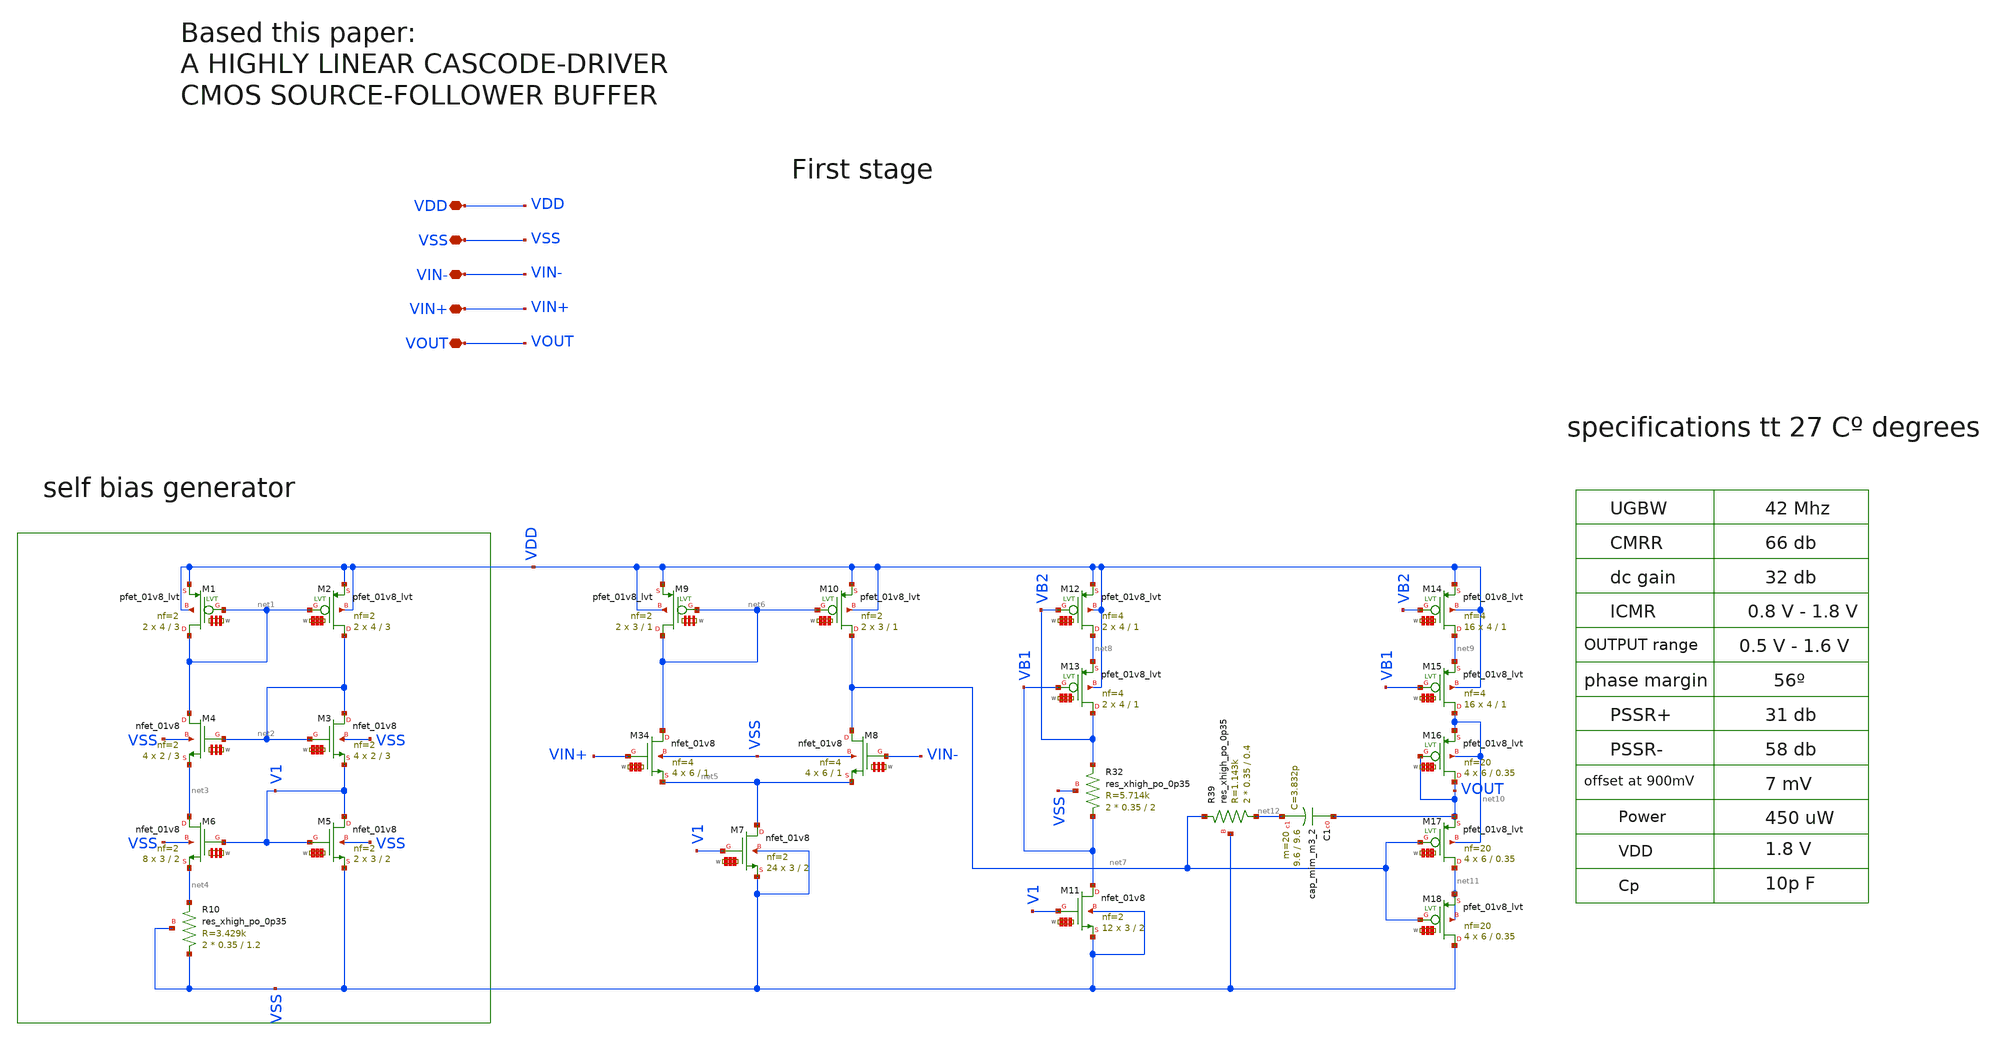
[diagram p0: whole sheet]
** sch_path: my_ip/LIB/Sky130A/single ended amplifiers/VA003_NMOS_1.8_sky130A.sch
**.subckt VA003_NMOS_1.8_sky130A VDD VSS VIN- VIN+ VOUT
*.iopin VDD
*.iopin VSS
*.iopin VIN-
*.iopin VIN+
*.iopin VOUT
XR10 VSS net4 VSS sky130_fd_pr__res_xhigh_po_0p35 L=1.2 mult=2 m=2
XM4 net1 net2 net3 VSS sky130_fd_pr__nfet_01v8 L=3 W='2 * 2 ' nf=2 ad='int((2 + 1)/2) * 2 / 2 * 0.29'
+ as='int((2 + 2)/2) * 2 / 2 * 0.29' pd='2*int((2 + 1)/2) * (2 / 2 + 0.29)' ps='2*int((2 + 2)/2) * (2 / 2 + 0.29)'
+ nrd='0.29 / 2 ' nrs='0.29 / 2 ' sa=0 sb=0 sd=0 mult=4 m=4
XM3 net2 net2 V1 VSS sky130_fd_pr__nfet_01v8 L=3 W='2 * 2 ' nf=2 ad='int((2 + 1)/2) * 2 / 2 * 0.29' as='int((2 + 2)/2) * 2 / 2 * 0.29'
+ pd='2*int((2 + 1)/2) * (2 / 2 + 0.29)' ps='2*int((2 + 2)/2) * (2 / 2 + 0.29)' nrd='0.29 / 2 ' nrs='0.29 / 2 '
+ sa=0 sb=0 sd=0 mult=4 m=4
XM6 net3 V1 net4 VSS sky130_fd_pr__nfet_01v8 L=2 W='3 * 2 ' nf=2 ad='int((2 + 1)/2) * 3 / 2 * 0.29' as='int((2 + 2)/2) * 3 / 2 * 0.29'
+ pd='2*int((2 + 1)/2) * (3 / 2 + 0.29)' ps='2*int((2 + 2)/2) * (3 / 2 + 0.29)' nrd='0.29 / 3 ' nrs='0.29 / 3 '
+ sa=0 sb=0 sd=0 mult=8 m=8
XM5 V1 V1 VSS VSS sky130_fd_pr__nfet_01v8 L=2 W='3 * 2 ' nf=2 ad='int((2 + 1)/2) * 3 / 2 * 0.29' as='int((2 + 2)/2) * 3 / 2 * 0.29'
+ pd='2*int((2 + 1)/2) * (3 / 2 + 0.29)' ps='2*int((2 + 2)/2) * (3 / 2 + 0.29)' nrd='0.29 / 3 ' nrs='0.29 / 3 '
+ sa=0 sb=0 sd=0 mult=2 m=2
XM2 net2 net1 VDD VDD sky130_fd_pr__pfet_01v8_lvt L=3 W='4 * 2 ' nf=2 ad='int((2 + 1)/2) * 4 / 2 * 0.29'
+ as='int((2 + 2)/2) * 4 / 2 * 0.29' pd='2*int((2 + 1)/2) * (4 / 2 + 0.29)' ps='2*int((2 + 2)/2) * (4 / 2 + 0.29)'
+ nrd='0.29 / 4 ' nrs='0.29 / 4 ' sa=0 sb=0 sd=0 mult=2 m=2
XM1 net1 net1 VDD VDD sky130_fd_pr__pfet_01v8_lvt L=3 W='4 * 2 ' nf=2 ad='int((2 + 1)/2) * 4 / 2 * 0.29'
+ as='int((2 + 2)/2) * 4 / 2 * 0.29' pd='2*int((2 + 1)/2) * (4 / 2 + 0.29)' ps='2*int((2 + 2)/2) * (4 / 2 + 0.29)'
+ nrd='0.29 / 4 ' nrs='0.29 / 4 ' sa=0 sb=0 sd=0 mult=2 m=2
XM7 net5 V1 VSS VSS sky130_fd_pr__nfet_01v8 L=2 W='3 * 2 ' nf=2 ad='int((2 + 1)/2) * 3 / 2 * 0.29' as='int((2 + 2)/2) * 3 / 2 * 0.29'
+ pd='2*int((2 + 1)/2) * (3 / 2 + 0.29)' ps='2*int((2 + 2)/2) * (3 / 2 + 0.29)' nrd='0.29 / 3 ' nrs='0.29 / 3 '
+ sa=0 sb=0 sd=0 mult=24 m=24
XM34 net6 VIN+ net5 VSS sky130_fd_pr__nfet_01v8 L=1 W='6 * 4 ' nf=4 ad='int((4 + 1)/2) * 6 / 4 * 0.29'
+ as='int((4 + 2)/2) * 6 / 4 * 0.29' pd='2*int((4 + 1)/2) * (6 / 4 + 0.29)' ps='2*int((4 + 2)/2) * (6 / 4 + 0.29)'
+ nrd='0.29 / 6 ' nrs='0.29 / 6 ' sa=0 sb=0 sd=0 mult=4 m=4
XM8 net7 VIN- net5 VSS sky130_fd_pr__nfet_01v8 L=1 W='6 * 4 ' nf=4 ad='int((4 + 1)/2) * 6 / 4 * 0.29'
+ as='int((4 + 2)/2) * 6 / 4 * 0.29' pd='2*int((4 + 1)/2) * (6 / 4 + 0.29)' ps='2*int((4 + 2)/2) * (6 / 4 + 0.29)'
+ nrd='0.29 / 6 ' nrs='0.29 / 6 ' sa=0 sb=0 sd=0 mult=4 m=4
XM9 net6 net6 VDD VDD sky130_fd_pr__pfet_01v8_lvt L=1 W='3 * 2 ' nf=2 ad='int((2 + 1)/2) * 3 / 2 * 0.29'
+ as='int((2 + 2)/2) * 3 / 2 * 0.29' pd='2*int((2 + 1)/2) * (3 / 2 + 0.29)' ps='2*int((2 + 2)/2) * (3 / 2 + 0.29)'
+ nrd='0.29 / 3 ' nrs='0.29 / 3 ' sa=0 sb=0 sd=0 mult=2 m=2
XM10 net7 net6 VDD VDD sky130_fd_pr__pfet_01v8_lvt L=1 W='3 * 2 ' nf=2 ad='int((2 + 1)/2) * 3 / 2 * 0.29'
+ as='int((2 + 2)/2) * 3 / 2 * 0.29' pd='2*int((2 + 1)/2) * (3 / 2 + 0.29)' ps='2*int((2 + 2)/2) * (3 / 2 + 0.29)'
+ nrd='0.29 / 3 ' nrs='0.29 / 3 ' sa=0 sb=0 sd=0 mult=2 m=2
XM11 VB1 V1 VSS VSS sky130_fd_pr__nfet_01v8 L=2 W='3 * 2 ' nf=2 ad='int((2 + 1)/2) * 3 / 2 * 0.29' as='int((2 + 2)/2) * 3 / 2 * 0.29'
+ pd='2*int((2 + 1)/2) * (3 / 2 + 0.29)' ps='2*int((2 + 2)/2) * (3 / 2 + 0.29)' nrd='0.29 / 3 ' nrs='0.29 / 3 '
+ sa=0 sb=0 sd=0 mult=12 m=12
XR32 VB1 VB2 VSS sky130_fd_pr__res_xhigh_po_0p35 L=2 mult=2 m=2
XM13 VB2 VB1 net8 VDD sky130_fd_pr__pfet_01v8_lvt L=1 W='4 * 4 ' nf=4 ad='int((4 + 1)/2) * 4 / 4 * 0.29'
+ as='int((4 + 2)/2) * 4 / 4 * 0.29' pd='2*int((4 + 1)/2) * (4 / 4 + 0.29)' ps='2*int((4 + 2)/2) * (4 / 4 + 0.29)'
+ nrd='0.29 / 4 ' nrs='0.29 / 4 ' sa=0 sb=0 sd=0 mult=2 m=2
XM12 net8 VB2 VDD VDD sky130_fd_pr__pfet_01v8_lvt L=1 W='4 * 4 ' nf=4 ad='int((4 + 1)/2) * 4 / 4 * 0.29'
+ as='int((4 + 2)/2) * 4 / 4 * 0.29' pd='2*int((4 + 1)/2) * (4 / 4 + 0.29)' ps='2*int((4 + 2)/2) * (4 / 4 + 0.29)'
+ nrd='0.29 / 4 ' nrs='0.29 / 4 ' sa=0 sb=0 sd=0 mult=2 m=2
XM14 net9 VB2 VDD VDD sky130_fd_pr__pfet_01v8_lvt L=1 W='4 * 4 ' nf=4 ad='int((4 + 1)/2) * 4 / 4 * 0.29'
+ as='int((4 + 2)/2) * 4 / 4 * 0.29' pd='2*int((4 + 1)/2) * (4 / 4 + 0.29)' ps='2*int((4 + 2)/2) * (4 / 4 + 0.29)'
+ nrd='0.29 / 4 ' nrs='0.29 / 4 ' sa=0 sb=0 sd=0 mult=16 m=16
XM15 net10 VB1 net9 VDD sky130_fd_pr__pfet_01v8_lvt L=1 W='4 * 4 ' nf=4 ad='int((4 + 1)/2) * 4 / 4 * 0.29'
+ as='int((4 + 2)/2) * 4 / 4 * 0.29' pd='2*int((4 + 1)/2) * (4 / 4 + 0.29)' ps='2*int((4 + 2)/2) * (4 / 4 + 0.29)'
+ nrd='0.29 / 4 ' nrs='0.29 / 4 ' sa=0 sb=0 sd=0 mult=16 m=16
XM17 net11 net7 VOUT net10 sky130_fd_pr__pfet_01v8_lvt L=0.35 W='6 * 20 ' nf=20 ad='int((20 + 1)/2) * 6 / 20 * 0.29'
+ as='int((20 + 2)/2) * 6 / 20 * 0.29' pd='2*int((20 + 1)/2) * (6 / 20 + 0.29)' ps='2*int((20 + 2)/2) * (6 / 20 + 0.29)'
+ nrd='0.29 / 6 ' nrs='0.29 / 6 ' sa=0 sb=0 sd=0 mult=4 m=4
XM18 VSS net7 net11 net11 sky130_fd_pr__pfet_01v8_lvt L=0.35 W='6 * 20 ' nf=20 ad='int((20 + 1)/2) * 6 / 20 * 0.29'
+ as='int((20 + 2)/2) * 6 / 20 * 0.29' pd='2*int((20 + 1)/2) * (6 / 20 + 0.29)' ps='2*int((20 + 2)/2) * (6 / 20 + 0.29)'
+ nrd='0.29 / 6 ' nrs='0.29 / 6 ' sa=0 sb=0 sd=0 mult=4 m=4
XM16 VOUT VOUT net10 net10 sky130_fd_pr__pfet_01v8_lvt L=0.35 W='6 * 20 ' nf=20 ad='int((20 + 1)/2) * 6 / 20 * 0.29'
+ as='int((20 + 2)/2) * 6 / 20 * 0.29' pd='2*int((20 + 1)/2) * (6 / 20 + 0.29)' ps='2*int((20 + 2)/2) * (6 / 20 + 0.29)'
+ nrd='0.29 / 6 ' nrs='0.29 / 6 ' sa=0 sb=0 sd=0 mult=4 m=4
XR39 net12 net7 VSS sky130_fd_pr__res_xhigh_po_0p35 L=0.4 mult=2 m=2
XC1 VOUT net12 sky130_fd_pr__cap_mim_m3_2 W=9.6 L=9.6 MF=20 m=20
**.ends
.end
